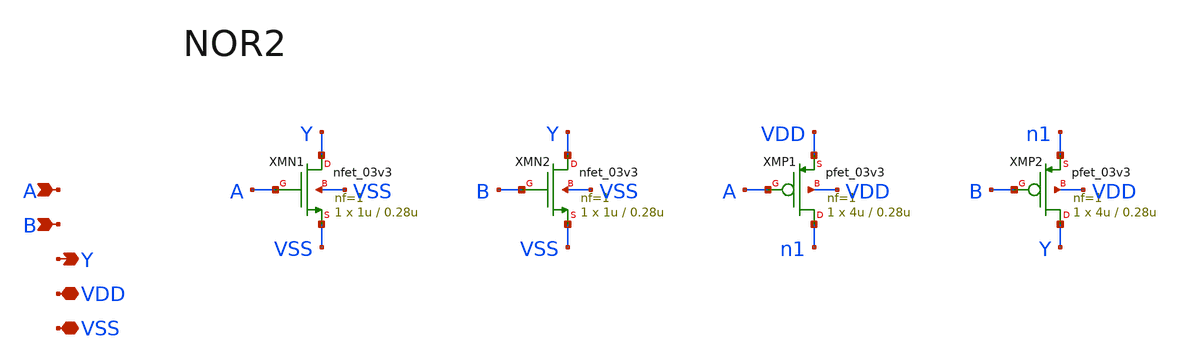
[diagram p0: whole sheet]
** sch_path: v1_claude/xschem/nor2.sch
**.subckt nor2 A B Y VDD VSS
*.ipin A
*.ipin B
*.opin Y
*.iopin VDD
*.iopin VSS
XMN1 Y A VSS VSS nfet_03v3 L=0.28u W=1u nf=1 ad='int((nf+1)/2) * W/nf * 0.18u' as='int((nf+2)/2) * W/nf * 0.18u'
+ pd='2*int((nf+1)/2) * (W/nf + 0.18u)' ps='2*int((nf+2)/2) * (W/nf + 0.18u)' nrd='0.18u / W' nrs='0.18u / W'
+ sa=0 sb=0 sd=0 m=1
XMN2 Y B VSS VSS nfet_03v3 L=0.28u W=1u nf=1 ad='int((nf+1)/2) * W/nf * 0.18u' as='int((nf+2)/2) * W/nf * 0.18u'
+ pd='2*int((nf+1)/2) * (W/nf + 0.18u)' ps='2*int((nf+2)/2) * (W/nf + 0.18u)' nrd='0.18u / W' nrs='0.18u / W'
+ sa=0 sb=0 sd=0 m=1
XMP1 n1 A VDD VDD pfet_03v3 L=0.28u W=4u nf=1 ad='int((nf+1)/2) * W/nf * 0.18u' as='int((nf+2)/2) * W/nf * 0.18u'
+ pd='2*int((nf+1)/2) * (W/nf + 0.18u)' ps='2*int((nf+2)/2) * (W/nf + 0.18u)' nrd='0.18u / W' nrs='0.18u / W'
+ sa=0 sb=0 sd=0 m=1
XMP2 Y B n1 VDD pfet_03v3 L=0.28u W=4u nf=1 ad='int((nf+1)/2) * W/nf * 0.18u' as='int((nf+2)/2) * W/nf * 0.18u'
+ pd='2*int((nf+1)/2) * (W/nf + 0.18u)' ps='2*int((nf+2)/2) * (W/nf + 0.18u)' nrd='0.18u / W' nrs='0.18u / W'
+ sa=0 sb=0 sd=0 m=1
**.ends
.end
